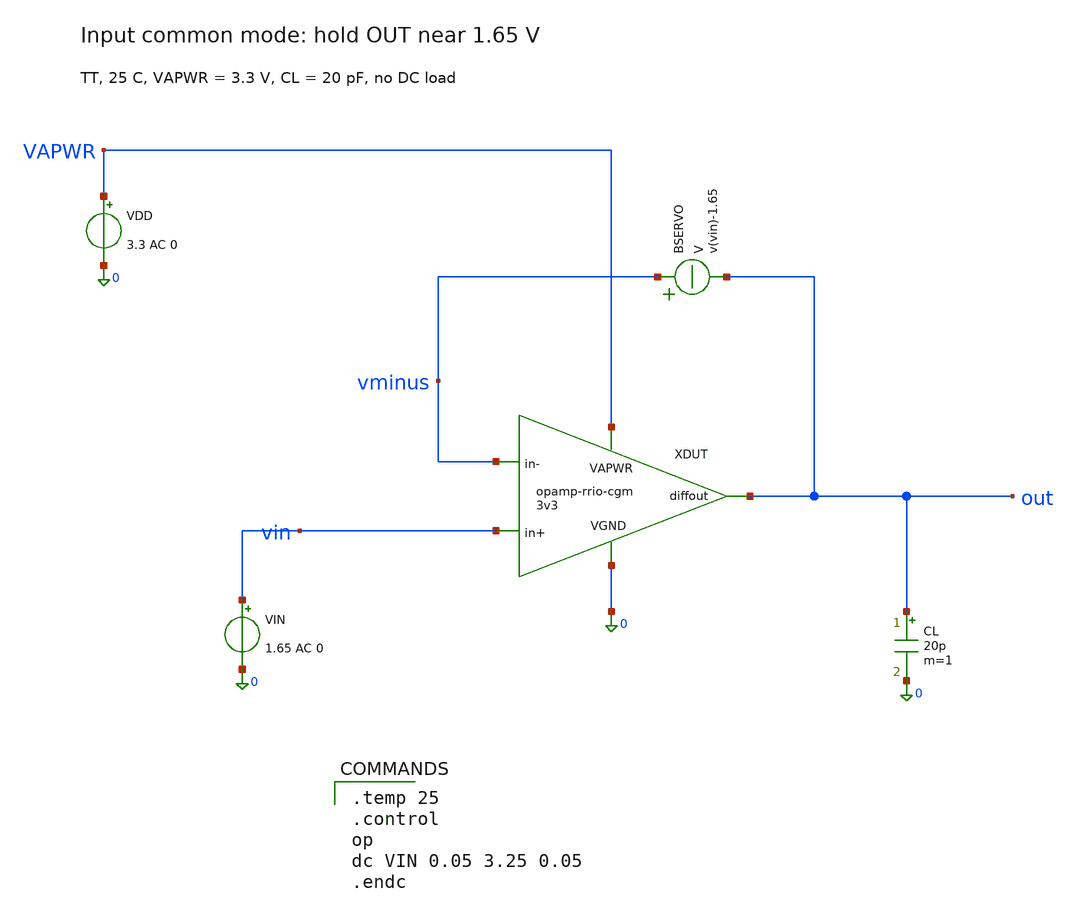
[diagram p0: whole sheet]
** sch_path: docs/simulation/xschem/bench-commonmode.sch
**.subckt bench-commonmode
XDUT VAPWR out vin vminus 0 opamp-rrio-cgm-3v3
VDD VAPWR 0 3.3 AC 0
VIN vin 0 1.65 AC 0
CL out 0 20p m=1
BSERVO vminus out V = v(vin)-1.65
**** begin user architecture code
 .lib $::SKYWATER_MODELS/sky130.lib.spice tt

.temp 25
.control
op
dc VIN 0.05 3.25 0.05
.endc

**** end user architecture code
**.ends
.end
